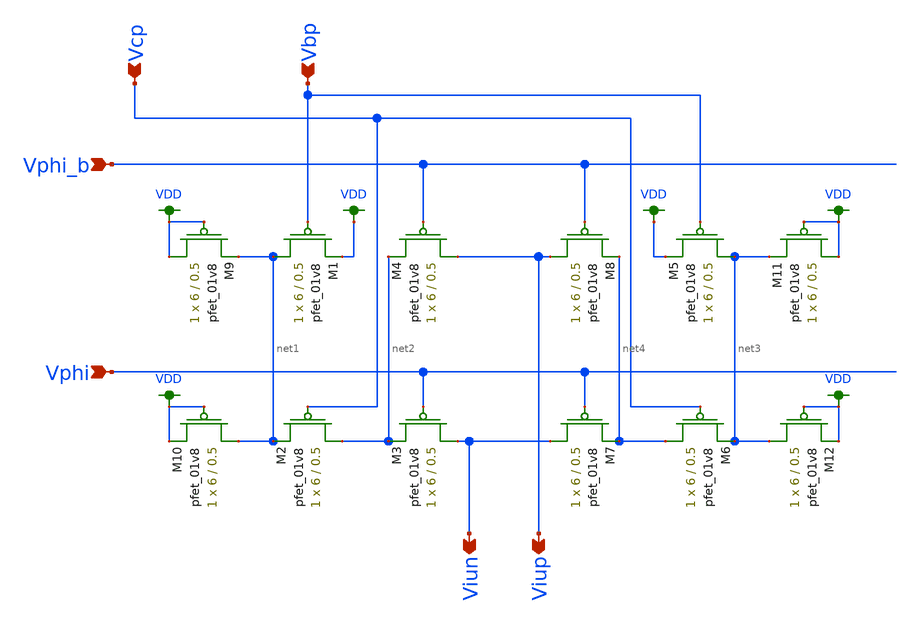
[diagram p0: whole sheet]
** sch_path: simulation/archived/dac_unit_lds_v2.sch
**.subckt dac_unit_lds_v2 Vphi Vbp Vcp Viun Viup Vphi_b
*.ipin Vphi
*.ipin Vbp
*.ipin Vcp
*.opin Viun
*.opin Viup
*.ipin Vphi_b
XM1 net1 Vbp VDD VDD sky130_fd_pr__pfet_01v8 L=0.5 W=6 nf=1 ad='int((nf+1)/2) * W/nf * 0.29' as='int((nf+2)/2) * W/nf * 0.29'
+ pd='2*int((nf+1)/2) * (W/nf + 0.29)' ps='2*int((nf+2)/2) * (W/nf + 0.29)' nrd='0.29 / W' nrs='0.29 / W'
+ sa=0 sb=0 sd=0 mult=1 m=1
XM2 net2 Vcp net1 VDD sky130_fd_pr__pfet_01v8 L=0.5 W=6 nf=1 ad='int((nf+1)/2) * W/nf * 0.29' as='int((nf+2)/2) * W/nf * 0.29'
+ pd='2*int((nf+1)/2) * (W/nf + 0.29)' ps='2*int((nf+2)/2) * (W/nf + 0.29)' nrd='0.29 / W' nrs='0.29 / W'
+ sa=0 sb=0 sd=0 mult=1 m=1
XM3 Viun Vphi net2 VDD sky130_fd_pr__pfet_01v8 L=0.5 W=6 nf=1 ad='int((nf+1)/2) * W/nf * 0.29' as='int((nf+2)/2) * W/nf * 0.29'
+ pd='2*int((nf+1)/2) * (W/nf + 0.29)' ps='2*int((nf+2)/2) * (W/nf + 0.29)' nrd='0.29 / W' nrs='0.29 / W'
+ sa=0 sb=0 sd=0 mult=1 m=1
XM4 Viup Vphi_b net2 VDD sky130_fd_pr__pfet_01v8 L=0.5 W=6 nf=1 ad='int((nf+1)/2) * W/nf * 0.29' as='int((nf+2)/2) * W/nf * 0.29'
+ pd='2*int((nf+1)/2) * (W/nf + 0.29)' ps='2*int((nf+2)/2) * (W/nf + 0.29)' nrd='0.29 / W' nrs='0.29 / W'
+ sa=0 sb=0 sd=0 mult=1 m=1
XM5 net3 Vbp VDD VDD sky130_fd_pr__pfet_01v8 L=0.5 W=6 nf=1 ad='int((nf+1)/2) * W/nf * 0.29' as='int((nf+2)/2) * W/nf * 0.29'
+ pd='2*int((nf+1)/2) * (W/nf + 0.29)' ps='2*int((nf+2)/2) * (W/nf + 0.29)' nrd='0.29 / W' nrs='0.29 / W'
+ sa=0 sb=0 sd=0 mult=1 m=1
XM6 net4 Vcp net3 VDD sky130_fd_pr__pfet_01v8 L=0.5 W=6 nf=1 ad='int((nf+1)/2) * W/nf * 0.29' as='int((nf+2)/2) * W/nf * 0.29'
+ pd='2*int((nf+1)/2) * (W/nf + 0.29)' ps='2*int((nf+2)/2) * (W/nf + 0.29)' nrd='0.29 / W' nrs='0.29 / W'
+ sa=0 sb=0 sd=0 mult=1 m=1
XM7 Viun Vphi net4 VDD sky130_fd_pr__pfet_01v8 L=0.5 W=6 nf=1 ad='int((nf+1)/2) * W/nf * 0.29' as='int((nf+2)/2) * W/nf * 0.29'
+ pd='2*int((nf+1)/2) * (W/nf + 0.29)' ps='2*int((nf+2)/2) * (W/nf + 0.29)' nrd='0.29 / W' nrs='0.29 / W'
+ sa=0 sb=0 sd=0 mult=1 m=1
XM8 Viup Vphi_b net4 VDD sky130_fd_pr__pfet_01v8 L=0.5 W=6 nf=1 ad='int((nf+1)/2) * W/nf * 0.29' as='int((nf+2)/2) * W/nf * 0.29'
+ pd='2*int((nf+1)/2) * (W/nf + 0.29)' ps='2*int((nf+2)/2) * (W/nf + 0.29)' nrd='0.29 / W' nrs='0.29 / W'
+ sa=0 sb=0 sd=0 mult=1 m=1
XM9 VDD VDD net1 VDD sky130_fd_pr__pfet_01v8 L=0.5 W=6 nf=1 ad='int((nf+1)/2) * W/nf * 0.29' as='int((nf+2)/2) * W/nf * 0.29'
+ pd='2*int((nf+1)/2) * (W/nf + 0.29)' ps='2*int((nf+2)/2) * (W/nf + 0.29)' nrd='0.29 / W' nrs='0.29 / W'
+ sa=0 sb=0 sd=0 mult=1 m=1
XM10 net1 VDD VDD VDD sky130_fd_pr__pfet_01v8 L=0.5 W=6 nf=1 ad='int((nf+1)/2) * W/nf * 0.29' as='int((nf+2)/2) * W/nf * 0.29'
+ pd='2*int((nf+1)/2) * (W/nf + 0.29)' ps='2*int((nf+2)/2) * (W/nf + 0.29)' nrd='0.29 / W' nrs='0.29 / W'
+ sa=0 sb=0 sd=0 mult=1 m=1
XM11 VDD VDD net3 VDD sky130_fd_pr__pfet_01v8 L=0.5 W=6 nf=1 ad='int((nf+1)/2) * W/nf * 0.29' as='int((nf+2)/2) * W/nf * 0.29'
+ pd='2*int((nf+1)/2) * (W/nf + 0.29)' ps='2*int((nf+2)/2) * (W/nf + 0.29)' nrd='0.29 / W' nrs='0.29 / W'
+ sa=0 sb=0 sd=0 mult=1 m=1
XM12 net3 VDD VDD VDD sky130_fd_pr__pfet_01v8 L=0.5 W=6 nf=1 ad='int((nf+1)/2) * W/nf * 0.29' as='int((nf+2)/2) * W/nf * 0.29'
+ pd='2*int((nf+1)/2) * (W/nf + 0.29)' ps='2*int((nf+2)/2) * (W/nf + 0.29)' nrd='0.29 / W' nrs='0.29 / W'
+ sa=0 sb=0 sd=0 mult=1 m=1
**.ends
.GLOBAL VDD
.end
